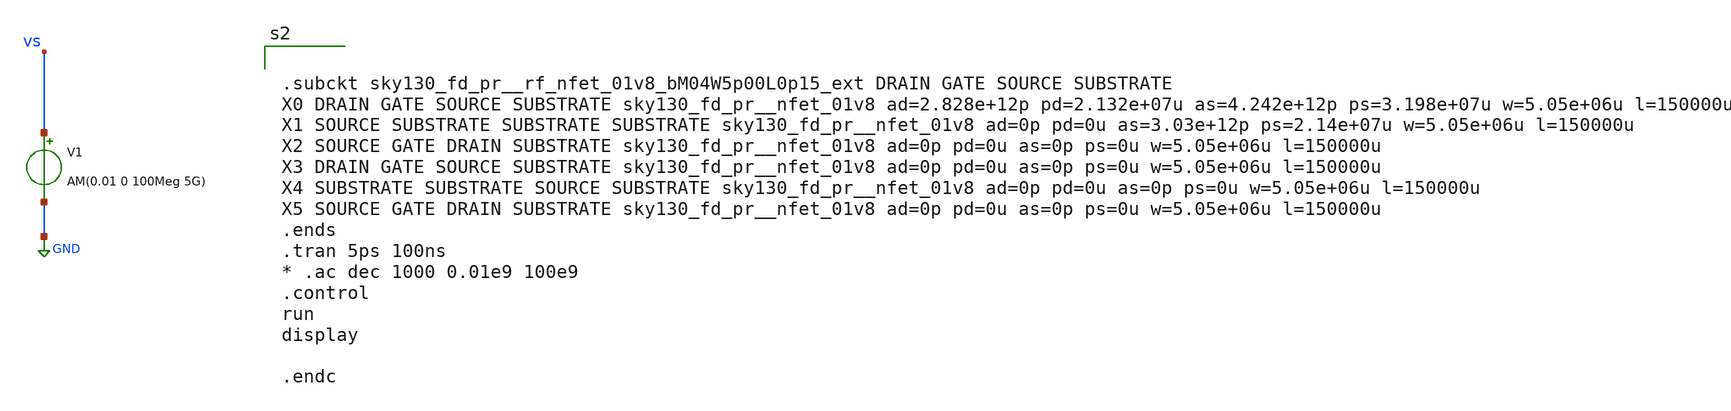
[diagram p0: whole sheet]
** sch_path: xschem/AM_signal_source.sch
**.subckt AM_signal_source
V1 vs GND AM(0.01 0 100Meg 5G)
**** begin user architecture code
.lib $::SKYWATER_MODELS/sky130.lib.spice tt
* .include $::PDKPATH/libs.ref/sky130_fd_sc_hvl/spice/sky130_fd_sc_hvl.spice



.subckt sky130_fd_pr__rf_nfet_01v8_bM04W5p00L0p15_ext DRAIN GATE SOURCE SUBSTRATE
X0 DRAIN GATE SOURCE SUBSTRATE sky130_fd_pr__nfet_01v8 ad=2.828e+12p pd=2.132e+07u as=4.242e+12p
+ ps=3.198e+07u w=5.05e+06u l=150000u
X1 SOURCE SUBSTRATE SUBSTRATE SUBSTRATE sky130_fd_pr__nfet_01v8 ad=0p pd=0u as=3.03e+12p
+ ps=2.14e+07u w=5.05e+06u l=150000u
X2 SOURCE GATE DRAIN SUBSTRATE sky130_fd_pr__nfet_01v8 ad=0p pd=0u as=0p ps=0u w=5.05e+06u l=150000u
X3 DRAIN GATE SOURCE SUBSTRATE sky130_fd_pr__nfet_01v8 ad=0p pd=0u as=0p ps=0u w=5.05e+06u l=150000u
X4 SUBSTRATE SUBSTRATE SOURCE SUBSTRATE sky130_fd_pr__nfet_01v8 ad=0p pd=0u as=0p ps=0u w=5.05e+06u
+ l=150000u
X5 SOURCE GATE DRAIN SUBSTRATE sky130_fd_pr__nfet_01v8 ad=0p pd=0u as=0p ps=0u w=5.05e+06u l=150000u
.ends
.tran 5ps 100ns
* .ac dec 1000 0.01e9 100e9
.control
run
display

.endc


**** end user architecture code
**.ends
.GLOBAL GND
.end
